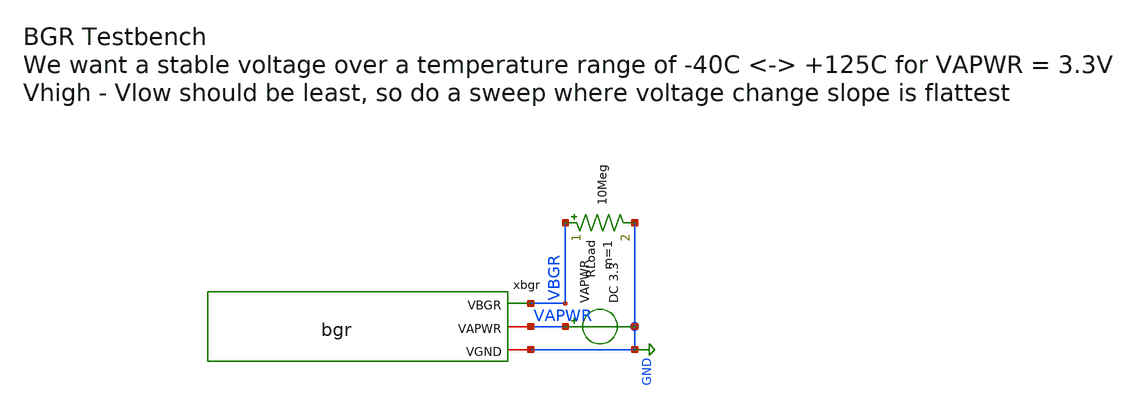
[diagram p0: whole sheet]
** sch_path: xschem/tb_bgr.sch
**.subckt tb_bgr
VAPWR VAPWR GND DC 3.3
xbgr VBGR VAPWR GND bgr
RLoad VBGR GND 10Meg m=1
**** begin user architecture code


.param sw_stat_global=0  ; enable statistical variation (0 = OFF, 1 = ON)
.param mc_skew=1         ; MOS variation scale factor (1 = Nominal)
.param res_mc_skew=1     ; resistor variation scale factor (1 = Nominal)
.param fnoicor=0         ; flicker noise model selector
.param sw_stat_mismatch=0
.lib /foss/pdks/gf180mcuD/libs.tech/ngspice/sm141064.ngspice typical
.lib /foss/pdks/gf180mcuD/libs.tech/ngspice/sm141064.ngspice bjt_typical
.lib /foss/pdks/gf180mcuD/libs.tech/ngspice/sm141064.ngspice res_typical
.control
  dc TEMP -40 125 5
  display
  wrdata tb_bgr_temp_sweep.dat v(VBGR) v(xbgr.net1) v(xbgr.net2) v(xbgr.net3) v(xbgr.net4)
+ v(xbgr.xbgr_core.e2) v(xbgr.xbgr_core.e1)
  plot v(VBGR)
.endc


**** end user architecture code
**.ends

* expanding   symbol:  bgr.sym # of pins=3
** sym_path: xschem/bgr.sym
** sch_path: xschem/bgr.sch
.subckt bgr VBGR VAPWR VGND
*.iopin VAPWR
*.iopin VGND
*.opin VBGR
xbgr_core net4 VAPWR net3 net1 net2 VBGR VGND bgr_core_without_amp
xbgr_amp net4 VAPWR net1 net2 net3 VGND bgr_error_amp
xbgr_ov_clamp net4 VBGR net3 VGND bgr_ov_clamp
.ends


* expanding   symbol:  bgr_core_without_amp.sym # of pins=7
** sym_path: xschem/bgr_core_without_amp.sym
** sch_path: xschem/bgr_core_without_amp.sch
.subckt bgr_core_without_amp BIAS_P VAPWR VCTRL VN2 VN1 VBGR VGND
*.iopin VGND
*.iopin VAPWR
*.opin VBGR
*.ipin VCTRL
*.opin BIAS_P
*.opin VN1
*.opin VN2
XQ1 VN1 VBGR E1 VBGR npn_05p00x05p00 m=1
XQ2 VN2 VBGR E2 VBGR npn_05p00x05p00 m=8
XR1 E1 E2 VGND ppolyf_u_3k r_width=1.18e-6 r_length=1e-6 m=1
XR2 VGND E1 VGND ppolyf_u_3k r_width=1e-6 r_length=25e-6 m=1
XR3 VGND VBGR VGND ppolyf_u_3k r_width=1e-6 r_length=50e-6 m=1
XM1 VN2 VCTRL VAPWR VAPWR pfet_03v3 L=4u W=8u nf=1 ad='int((nf+1)/2) * W/nf * 0.18u' as='int((nf+2)/2) * W/nf * 0.18u'
+ pd='2*int((nf+1)/2) * (W/nf + 0.18u)' ps='2*int((nf+2)/2) * (W/nf + 0.18u)' nrd='0.18u / W' nrs='0.18u / W'
+ sa=0 sb=0 sd=0 m=1
XM2 VN1 VCTRL VAPWR VAPWR pfet_03v3 L=4u W=8u nf=1 ad='int((nf+1)/2) * W/nf * 0.18u' as='int((nf+2)/2) * W/nf * 0.18u'
+ pd='2*int((nf+1)/2) * (W/nf + 0.18u)' ps='2*int((nf+2)/2) * (W/nf + 0.18u)' nrd='0.18u / W' nrs='0.18u / W'
+ sa=0 sb=0 sd=0 m=1
XM3 NBIAS_N VCTRL VAPWR VAPWR pfet_03v3 L=4u W=2u nf=1 ad='int((nf+1)/2) * W/nf * 0.18u' as='int((nf+2)/2) * W/nf * 0.18u'
+ pd='2*int((nf+1)/2) * (W/nf + 0.18u)' ps='2*int((nf+2)/2) * (W/nf + 0.18u)' nrd='0.18u / W' nrs='0.18u / W'
+ sa=0 sb=0 sd=0 m=1
XM4 VBGR VCTRL VAPWR VAPWR pfet_03v3 L=4u W=64u nf=1 ad='int((nf+1)/2) * W/nf * 0.18u' as='int((nf+2)/2) * W/nf * 0.18u'
+ pd='2*int((nf+1)/2) * (W/nf + 0.18u)' ps='2*int((nf+2)/2) * (W/nf + 0.18u)' nrd='0.18u / W' nrs='0.18u / W'
+ sa=0 sb=0 sd=0 m=1
XM5 BIAS_P BIAS_P VAPWR VAPWR pfet_03v3 L=4u W=1u nf=1 ad='int((nf+1)/2) * W/nf * 0.18u' as='int((nf+2)/2) * W/nf * 0.18u'
+ pd='2*int((nf+1)/2) * (W/nf + 0.18u)' ps='2*int((nf+2)/2) * (W/nf + 0.18u)' nrd='0.18u / W' nrs='0.18u / W'
+ sa=0 sb=0 sd=0 m=1
XM6 BIAS_P NBIAS_N VGND VGND nfet_03v3 L=4u W=1u nf=1 ad='int((nf+1)/2) * W/nf * 0.18u' as='int((nf+2)/2) * W/nf * 0.18u'
+ pd='2*int((nf+1)/2) * (W/nf + 0.18u)' ps='2*int((nf+2)/2) * (W/nf + 0.18u)' nrd='0.18u / W' nrs='0.18u / W'
+ sa=0 sb=0 sd=0 m=1
XM7 NBIAS_N NBIAS_N VGND VGND nfet_03v3 L=4u W=1u nf=1 ad='int((nf+1)/2) * W/nf * 0.18u' as='int((nf+2)/2) * W/nf * 0.18u'
+ pd='2*int((nf+1)/2) * (W/nf + 0.18u)' ps='2*int((nf+2)/2) * (W/nf + 0.18u)' nrd='0.18u / W' nrs='0.18u / W'
+ sa=0 sb=0 sd=0 m=1
.ends


* expanding   symbol:  bgr_error_amp.sym # of pins=6
** sym_path: xschem/bgr_error_amp.sym
** sch_path: xschem/bgr_error_amp.sch
.subckt bgr_error_amp BIAS_P VAPWR VIN_P VIN_N VOUT VGND
*.ipin VIN_P
*.ipin VIN_N
*.ipin BIAS_P
*.iopin VAPWR
*.iopin VGND
*.opin VOUT
XMDIFF_P net1 VIN_P TAIL_P VAPWR pfet_03v3 L=0.28u W=0.22u nf=1 ad='int((nf+1)/2) * W/nf * 0.18u' as='int((nf+2)/2) * W/nf * 0.18u'
+ pd='2*int((nf+1)/2) * (W/nf + 0.18u)' ps='2*int((nf+2)/2) * (W/nf + 0.18u)' nrd='0.18u / W' nrs='0.18u / W'
+ sa=0 sb=0 sd=0 m=1
XMDIFF_N VOUT VIN_N TAIL_P VAPWR pfet_03v3 L=0.28u W=0.22u nf=1 ad='int((nf+1)/2) * W/nf * 0.18u' as='int((nf+2)/2) * W/nf * 0.18u'
+ pd='2*int((nf+1)/2) * (W/nf + 0.18u)' ps='2*int((nf+2)/2) * (W/nf + 0.18u)' nrd='0.18u / W' nrs='0.18u / W'
+ sa=0 sb=0 sd=0 m=1
XMTAIL TAIL_P BIAS_P VAPWR VAPWR pfet_03v3 L=0.28u W=0.22u nf=1 ad='int((nf+1)/2) * W/nf * 0.18u' as='int((nf+2)/2) * W/nf * 0.18u'
+ pd='2*int((nf+1)/2) * (W/nf + 0.18u)' ps='2*int((nf+2)/2) * (W/nf + 0.18u)' nrd='0.18u / W' nrs='0.18u / W'
+ sa=0 sb=0 sd=0 m=1
XMLOAD_REF net1 net1 VGND VGND nfet_03v3 L=0.28u W=0.22u nf=1 ad='int((nf+1)/2) * W/nf * 0.18u' as='int((nf+2)/2) * W/nf * 0.18u'
+ pd='2*int((nf+1)/2) * (W/nf + 0.18u)' ps='2*int((nf+2)/2) * (W/nf + 0.18u)' nrd='0.18u / W' nrs='0.18u / W'
+ sa=0 sb=0 sd=0 m=1
XMLOAD_OUT VOUT net1 VGND VGND nfet_03v3 L=0.28u W=0.22u nf=1 ad='int((nf+1)/2) * W/nf * 0.18u' as='int((nf+2)/2) * W/nf * 0.18u'
+ pd='2*int((nf+1)/2) * (W/nf + 0.18u)' ps='2*int((nf+2)/2) * (W/nf + 0.18u)' nrd='0.18u / W' nrs='0.18u / W'
+ sa=0 sb=0 sd=0 m=1
.ends


* expanding   symbol:  bgr_ov_clamp.sym # of pins=4
** sym_path: xschem/bgr_ov_clamp.sym
** sch_path: xschem/bgr_ov_clamp.sch
.subckt bgr_ov_clamp VAPWR VBGR VCTRL VGND
*.iopin VAPWR
*.iopin VGND
*.ipin VBGR
*.iopin VCTRL
XMOVDET_N OV_N VBGR VGND VGND nfet_03v3 L=1u W=0.3u nf=1 ad='int((nf+1)/2) * W/nf * 0.18u' as='int((nf+2)/2) * W/nf * 0.18u'
+ pd='2*int((nf+1)/2) * (W/nf + 0.18u)' ps='2*int((nf+2)/2) * (W/nf + 0.18u)' nrd='0.18u / W' nrs='0.18u / W'
+ sa=0 sb=0 sd=0 m=1
XMOVDET_P OV_N VBGR VAPWR VAPWR pfet_03v3 L=4u W=8u nf=1 ad='int((nf+1)/2) * W/nf * 0.18u' as='int((nf+2)/2) * W/nf * 0.18u'
+ pd='2*int((nf+1)/2) * (W/nf + 0.18u)' ps='2*int((nf+2)/2) * (W/nf + 0.18u)' nrd='0.18u / W' nrs='0.18u / W'
+ sa=0 sb=0 sd=0 m=1
XMOVCLAMP VCTRL OV_N VAPWR VAPWR pfet_03v3 L=8u W=0.5u nf=1 ad='int((nf+1)/2) * W/nf * 0.18u' as='int((nf+2)/2) * W/nf * 0.18u'
+ pd='2*int((nf+1)/2) * (W/nf + 0.18u)' ps='2*int((nf+2)/2) * (W/nf + 0.18u)' nrd='0.18u / W' nrs='0.18u / W'
+ sa=0 sb=0 sd=0 m=1
.ends

.GLOBAL GND
.end
